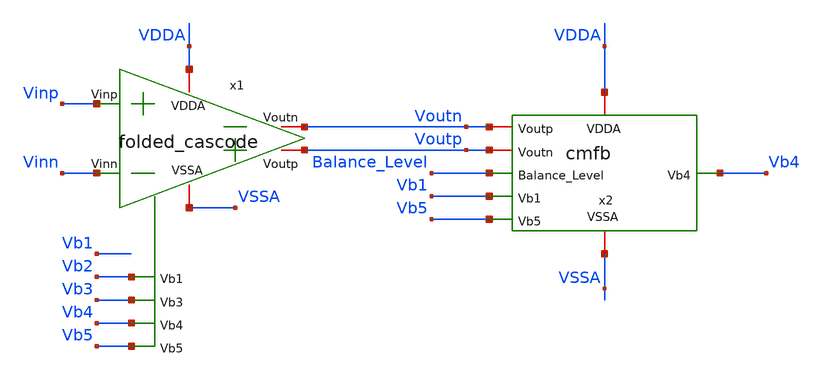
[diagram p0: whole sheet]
** sch_path: Folded_cascode/schematic/folded_cascode_cmfb.sch
**.subckt folded_cascode_cmfb
x1 VDDA VSSA Vinp Vinn Voutp Voutn Vb2 Vb3 Vb4 Vb5 folded_cascode
x2 VDDA VSSA Voutn Voutp Balance_Level Vb1 Vb4 Vb5 cmfb
**.ends
.end
